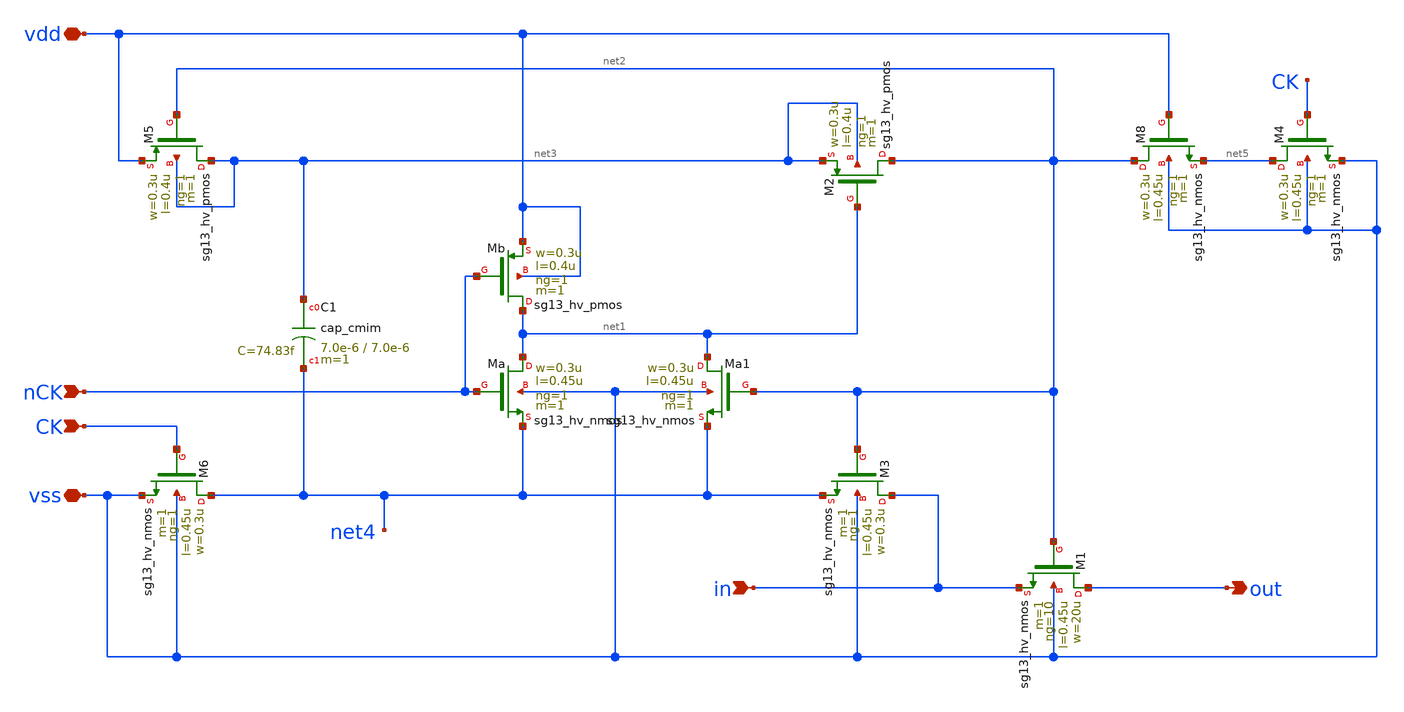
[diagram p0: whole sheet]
** sch_path: sal/b-switch.sch
**.subckt b-switch vdd nCK out vss CK in
*.iopin vdd
*.ipin nCK
*.opin out
*.iopin vss
*.ipin CK
*.ipin in
XM1 out net2 in vss sg13_hv_nmos w=20u l=0.45u ng=10 m=1 mm_ok=1
XM2 net2 net1 net3 net3 sg13_hv_pmos w=0.3u l=0.4u ng=1 m=1 mm_ok=1
XM3 in net2 net4 vss sg13_hv_nmos w=0.3u l=0.45u ng=1 m=1 mm_ok=1
XM4 net5 CK vss vss sg13_hv_nmos w=0.3u l=0.45u ng=1 m=1 mm_ok=1
XM5 net3 net2 vdd net3 sg13_hv_pmos w=0.3u l=0.4u ng=1 m=1 mm_ok=1
XM6 net4 CK vss vss sg13_hv_nmos w=0.3u l=0.45u ng=1 m=1 mm_ok=1
XMa net1 nCK net4 vss sg13_hv_nmos w=0.3u l=0.45u ng=1 m=1 mm_ok=1
XMb net1 nCK vdd vdd sg13_hv_pmos w=0.3u l=0.4u ng=1 m=1 mm_ok=1
XMa1 net1 net2 net4 vss sg13_hv_nmos w=0.3u l=0.45u ng=1 m=1 mm_ok=1
XM8 net2 vdd net5 vss sg13_hv_nmos w=0.3u l=0.45u ng=1 m=1 mm_ok=1
XC1 net3 net4 cap_cmim w=7.0e-6 l=7.0e-6 m=1 mm_ok=1
**.ends
.end
